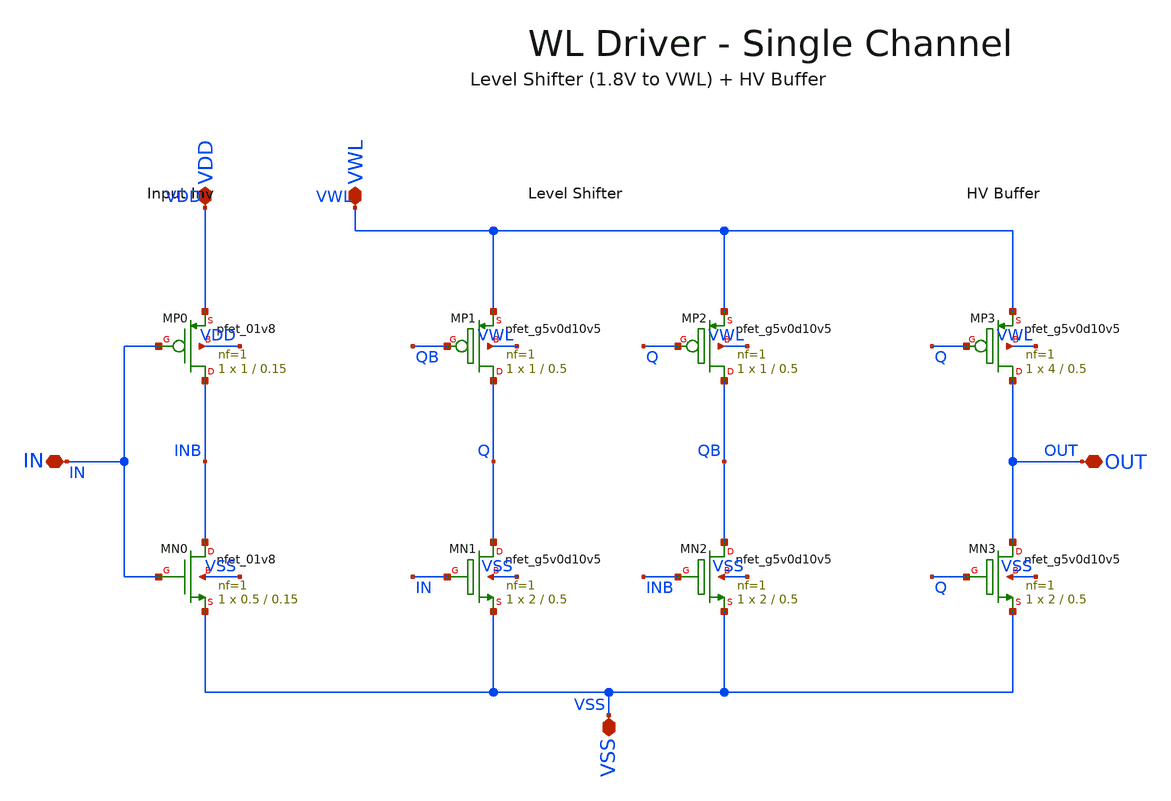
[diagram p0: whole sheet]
** sch_path: analog/xschem/xschem/wl_driver.sch
**.subckt wl_driver IN OUT VDD VWL VSS
*.iopin IN
*.iopin OUT
*.iopin VDD
*.iopin VWL
*.iopin VSS
XMP0 INB IN VDD VDD sky130_fd_pr__pfet_01v8 L=0.15 W=1 nf=1 ad='int((nf+1)/2) * W/nf * 0.29' as='int((nf+2)/2) * W/nf * 0.29'
+ pd='2*int((nf+1)/2) * (W/nf + 0.29)' ps='2*int((nf+2)/2) * (W/nf + 0.29)' nrd='0.29 / W' nrs='0.29 / W'
+ sa=0 sb=0 sd=0 mult=1 m=1
XMN0 INB IN VSS VSS sky130_fd_pr__nfet_01v8 L=0.15 W=0.5 nf=1 ad='int((1 + 1)/2) * 0.5 / 1 * 0.29' as='int((1 + 2)/2) * 0.5 / 1 * 0.29'
+ pd='2*int((1 + 1)/2) * (0.5 / 1 + 0.29)' ps='2*int((1 + 2)/2) * (0.5 / 1 + 0.29)' nrd='0.29 / 0.5 ' nrs='0.29 / 0.5 '
+ sa=0 sb=0 sd=0 mult=1 m=1
XMP1 Q QB VWL VWL sky130_fd_pr__pfet_g5v0d10v5 L=0.5 W=1 nf=1 ad='int((1 + 1)/2) * 1 / 1 * 0.29' as='int((1 + 2)/2) * 1 / 1 * 0.29'
+ pd='2*int((1 + 1)/2) * (1 / 1 + 0.29)' ps='2*int((1 + 2)/2) * (1 / 1 + 0.29)' nrd='0.29 / 1 ' nrs='0.29 / 1 '
+ sa=0 sb=0 sd=0 mult=1 m=1
XMN1 Q IN VSS VSS sky130_fd_pr__nfet_g5v0d10v5 L=0.5 W=2 nf=1 ad='int((1 + 1)/2) * 2 / 1 * 0.29' as='int((1 + 2)/2) * 2 / 1 * 0.29'
+ pd='2*int((1 + 1)/2) * (2 / 1 + 0.29)' ps='2*int((1 + 2)/2) * (2 / 1 + 0.29)' nrd='0.29 / 2 ' nrs='0.29 / 2 '
+ sa=0 sb=0 sd=0 mult=1 m=1
XMP2 QB Q VWL VWL sky130_fd_pr__pfet_g5v0d10v5 L=0.5 W=1 nf=1 ad='int((1 + 1)/2) * 1 / 1 * 0.29' as='int((1 + 2)/2) * 1 / 1 * 0.29'
+ pd='2*int((1 + 1)/2) * (1 / 1 + 0.29)' ps='2*int((1 + 2)/2) * (1 / 1 + 0.29)' nrd='0.29 / 1 ' nrs='0.29 / 1 '
+ sa=0 sb=0 sd=0 mult=1 m=1
XMN2 QB INB VSS VSS sky130_fd_pr__nfet_g5v0d10v5 L=0.5 W=2 nf=1 ad='int((1 + 1)/2) * 2 / 1 * 0.29' as='int((1 + 2)/2) * 2 / 1 * 0.29'
+ pd='2*int((1 + 1)/2) * (2 / 1 + 0.29)' ps='2*int((1 + 2)/2) * (2 / 1 + 0.29)' nrd='0.29 / 2 ' nrs='0.29 / 2 '
+ sa=0 sb=0 sd=0 mult=1 m=1
XMP3 OUT Q VWL VWL sky130_fd_pr__pfet_g5v0d10v5 L=0.5 W=4 nf=1 ad='int((1 + 1)/2) * 4 / 1 * 0.29' as='int((1 + 2)/2) * 4 / 1 * 0.29'
+ pd='2*int((1 + 1)/2) * (4 / 1 + 0.29)' ps='2*int((1 + 2)/2) * (4 / 1 + 0.29)' nrd='0.29 / 4 ' nrs='0.29 / 4 '
+ sa=0 sb=0 sd=0 mult=1 m=1
XMN3 OUT Q VSS VSS sky130_fd_pr__nfet_g5v0d10v5 L=0.5 W=2 nf=1 ad='int((1 + 1)/2) * 2 / 1 * 0.29' as='int((1 + 2)/2) * 2 / 1 * 0.29'
+ pd='2*int((1 + 1)/2) * (2 / 1 + 0.29)' ps='2*int((1 + 2)/2) * (2 / 1 + 0.29)' nrd='0.29 / 2 ' nrs='0.29 / 2 '
+ sa=0 sb=0 sd=0 mult=1 m=1
**.ends
.end
